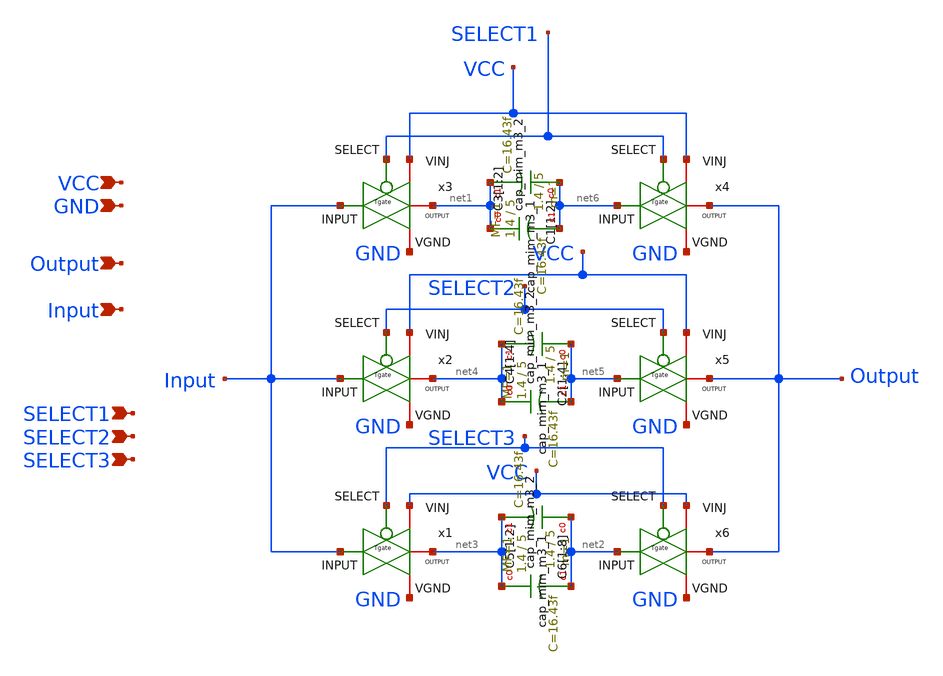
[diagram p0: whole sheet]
** sch_path: sky130_cells/Practice/Capacitor_Array/Schematic/CapArray.sch
**.subckt CapArray GND SELECT1 VCC SELECT2 SELECT3 Output Input
*.ipin GND
*.ipin SELECT1
*.ipin VCC
*.ipin SELECT2
*.ipin SELECT3
*.ipin Output
*.ipin Input
x1 VCC net3 SELECT3 Input GND Tgate
x2 VCC net4 SELECT2 Input GND Tgate
x3 VCC net1 SELECT1 Input GND Tgate
x4 VCC Output SELECT1 net6 GND Tgate
x5 VCC Output SELECT2 net5 GND Tgate
x6 VCC Output SELECT3 net2 GND Tgate
XC1[1] net6 net1 sky130_fd_pr__cap_mim_m3_1 W=1.4 L=5 MF=1 m=1
XC1[2] net6 net1 sky130_fd_pr__cap_mim_m3_1 W=1.4 L=5 MF=1 m=1
XC3[1] net1 net6 sky130_fd_pr__cap_mim_m3_2 W=1.4 L=5 MF=1 m=1
XC3[2] net1 net6 sky130_fd_pr__cap_mim_m3_2 W=1.4 L=5 MF=1 m=1
XC2[1] net5 net4 sky130_fd_pr__cap_mim_m3_1 W=1.4 L=5 MF=1 m=1
XC2[2] net5 net4 sky130_fd_pr__cap_mim_m3_1 W=1.4 L=5 MF=1 m=1
XC2[3] net5 net4 sky130_fd_pr__cap_mim_m3_1 W=1.4 L=5 MF=1 m=1
XC2[4] net5 net4 sky130_fd_pr__cap_mim_m3_1 W=1.4 L=5 MF=1 m=1
XC4[1] net4 net5 sky130_fd_pr__cap_mim_m3_2 W=1.4 L=5 MF=1 m=1
XC4[2] net4 net5 sky130_fd_pr__cap_mim_m3_2 W=1.4 L=5 MF=1 m=1
XC4[3] net4 net5 sky130_fd_pr__cap_mim_m3_2 W=1.4 L=5 MF=1 m=1
XC4[4] net4 net5 sky130_fd_pr__cap_mim_m3_2 W=1.4 L=5 MF=1 m=1
XC5[1] net3 net2 sky130_fd_pr__cap_mim_m3_2 W=1.4 L=5 MF=1 m=1
XC5[2] net3 net2 sky130_fd_pr__cap_mim_m3_2 W=1.4 L=5 MF=1 m=1
XC6[1] net2 net3 sky130_fd_pr__cap_mim_m3_1 W=1.4 L=5 MF=1 m=1
XC6[2] net2 net3 sky130_fd_pr__cap_mim_m3_1 W=1.4 L=5 MF=1 m=1
XC6[3] net2 net3 sky130_fd_pr__cap_mim_m3_1 W=1.4 L=5 MF=1 m=1
XC6[4] net2 net3 sky130_fd_pr__cap_mim_m3_1 W=1.4 L=5 MF=1 m=1
XC6[5] net2 net3 sky130_fd_pr__cap_mim_m3_1 W=1.4 L=5 MF=1 m=1
XC6[6] net2 net3 sky130_fd_pr__cap_mim_m3_1 W=1.4 L=5 MF=1 m=1
XC6[7] net2 net3 sky130_fd_pr__cap_mim_m3_1 W=1.4 L=5 MF=1 m=1
XC6[8] net2 net3 sky130_fd_pr__cap_mim_m3_1 W=1.4 L=5 MF=1 m=1
**.ends

* expanding   symbol:  sky130_cells/RDAC/Design/Tgate.sym # of pins=5
** sym_path: sky130_cells/RDAC/Design/Tgate.sym
** sch_path: sky130_cells/RDAC/Design/Tgate.sch
.subckt Tgate VINJ OUTPUT SELECT INPUT VGND
*.iopin VINJ
*.ipin SELECT
*.iopin INPUT
*.iopin OUTPUT
*.ipin VGND
XM5 net1 SELECT VGND VGND sky130_fd_pr__nfet_g5v0d10v5 L=0.5 W=0.42 nf=1 ad='int((1 + 1)/2) * 0.42 / 1 * 0.29'
+ as='int((1 + 2)/2) * 0.42 / 1 * 0.29' pd='2*int((1 + 1)/2) * (0.42 / 1 + 0.29)' ps='2*int((1 + 2)/2) * (0.42 / 1 + 0.29)'
+ nrd='0.29 / 0.42 ' nrs='0.29 / 0.42 ' sa=0 sb=0 sd=0 mult=1 m=1
XM1 net1 SELECT VINJ VINJ sky130_fd_pr__pfet_g5v0d10v5 L=0.5 W=0.42 nf=1 ad='int((1 + 1)/2) * 0.42 / 1 * 0.29'
+ as='int((1 + 2)/2) * 0.42 / 1 * 0.29' pd='2*int((1 + 1)/2) * (0.42 / 1 + 0.29)' ps='2*int((1 + 2)/2) * (0.42 / 1 + 0.29)'
+ nrd='0.29 / 0.42 ' nrs='0.29 / 0.42 ' sa=0 sb=0 sd=0 mult=1 m=1
XM2 INPUT net1 OUTPUT VINJ sky130_fd_pr__pfet_g5v0d10v5 L=0.5 W=0.42 nf=1 ad='int((1 + 1)/2) * 0.42 / 1 * 0.29'
+ as='int((1 + 2)/2) * 0.42 / 1 * 0.29' pd='2*int((1 + 1)/2) * (0.42 / 1 + 0.29)' ps='2*int((1 + 2)/2) * (0.42 / 1 + 0.29)'
+ nrd='0.29 / 0.42 ' nrs='0.29 / 0.42 ' sa=0 sb=0 sd=0 mult=1 m=1
XM3 OUTPUT SELECT INPUT VGND sky130_fd_pr__nfet_g5v0d10v5 L=0.5 W=0.42 nf=1 ad='int((1 + 1)/2) * 0.42 / 1 * 0.29'
+ as='int((1 + 2)/2) * 0.42 / 1 * 0.29' pd='2*int((1 + 1)/2) * (0.42 / 1 + 0.29)' ps='2*int((1 + 2)/2) * (0.42 / 1 + 0.29)'
+ nrd='0.29 / 0.42 ' nrs='0.29 / 0.42 ' sa=0 sb=0 sd=0 mult=1 m=1
.ends

.end
